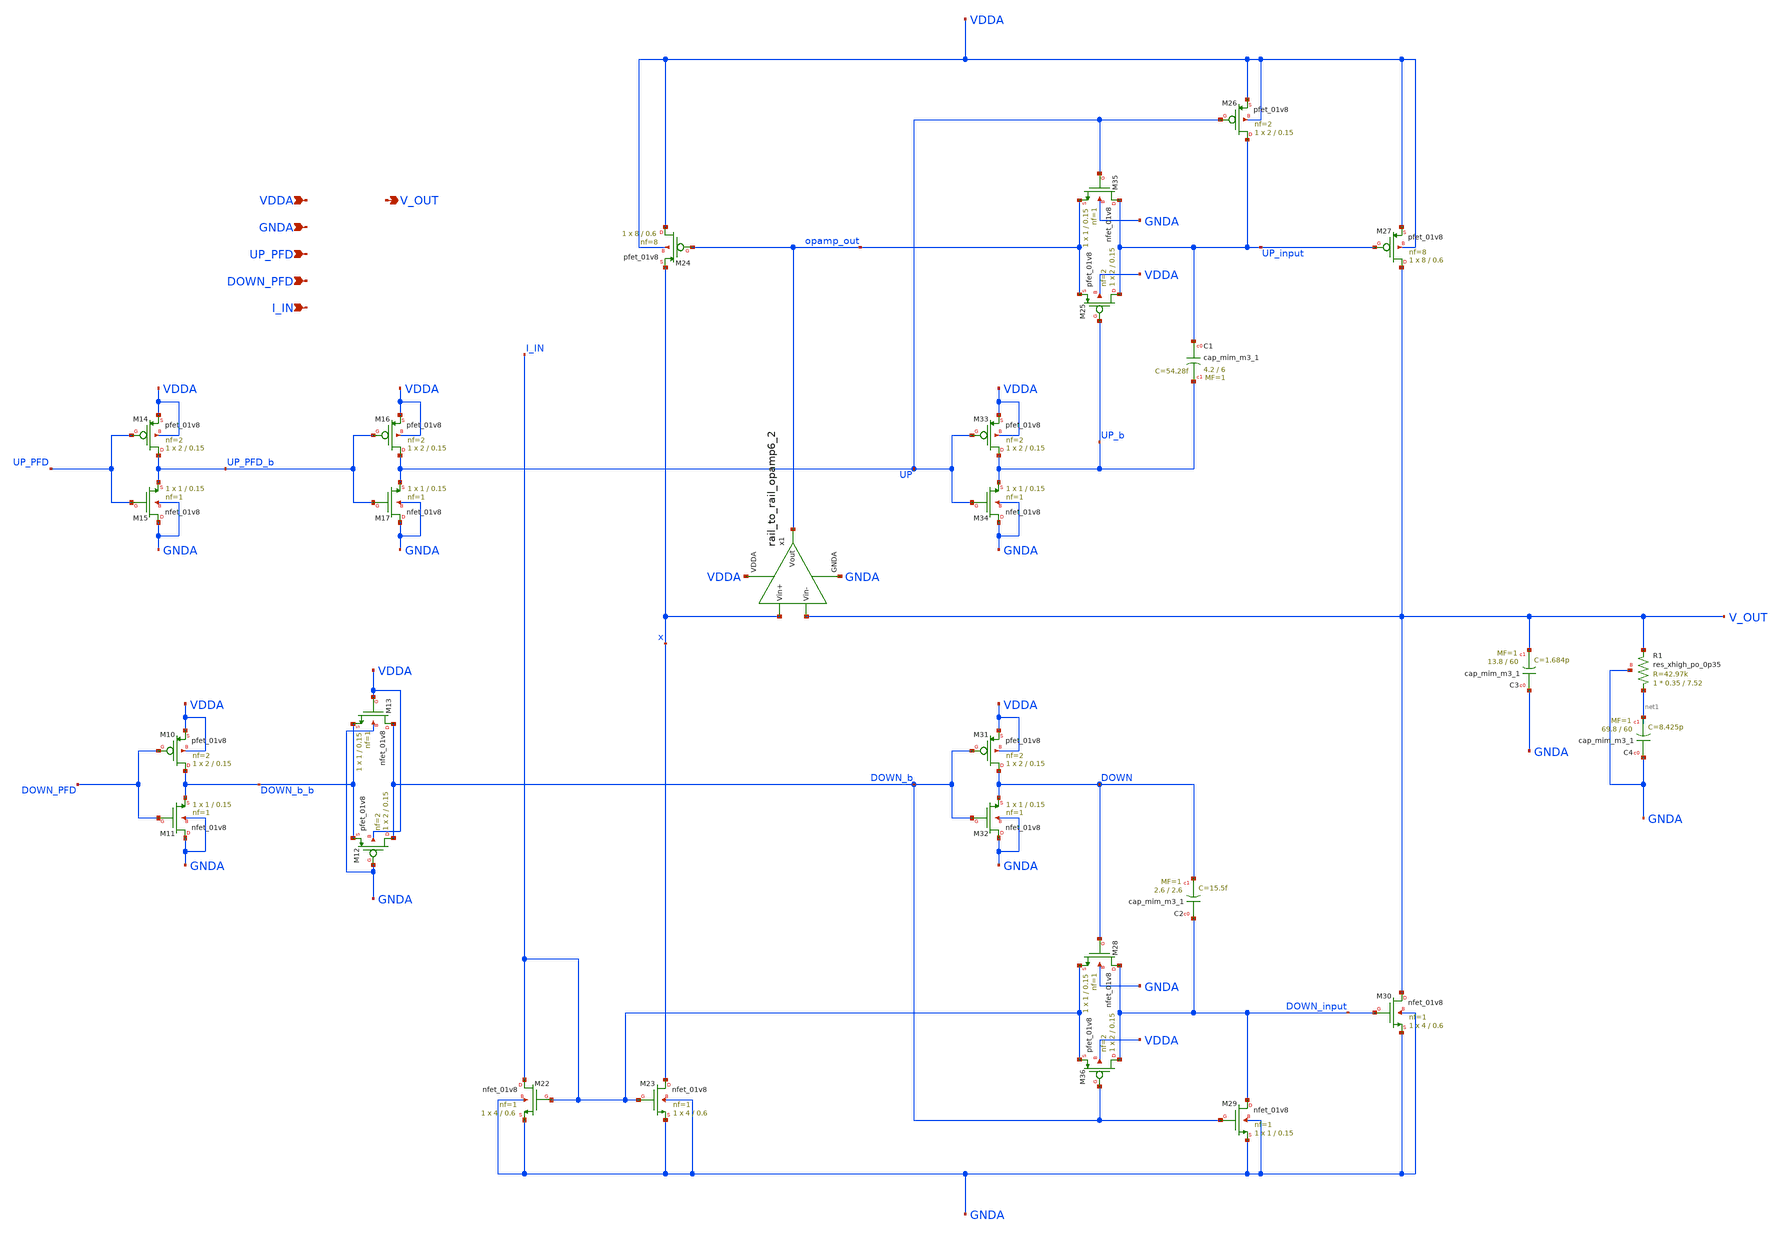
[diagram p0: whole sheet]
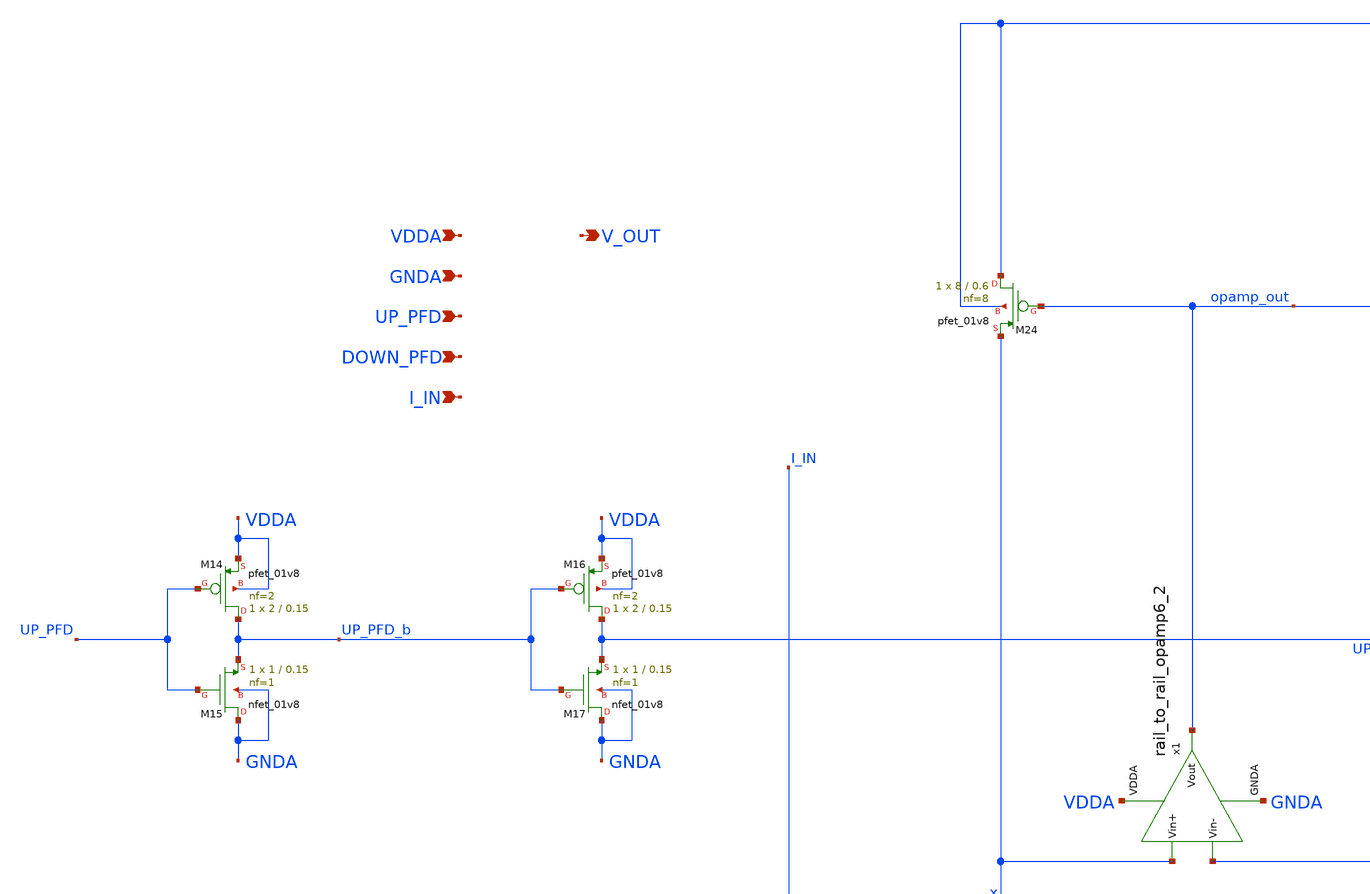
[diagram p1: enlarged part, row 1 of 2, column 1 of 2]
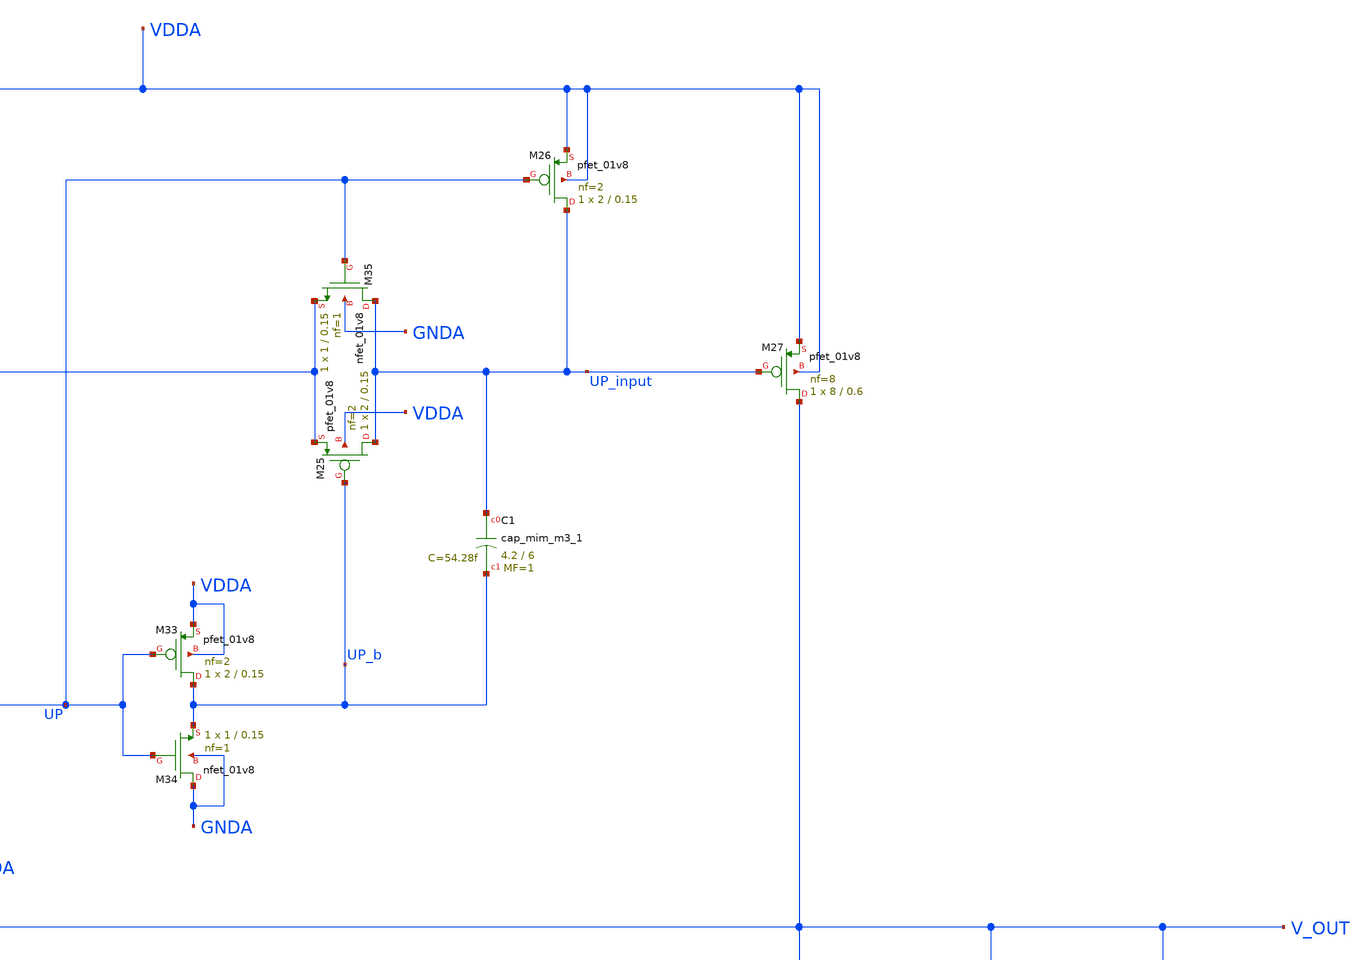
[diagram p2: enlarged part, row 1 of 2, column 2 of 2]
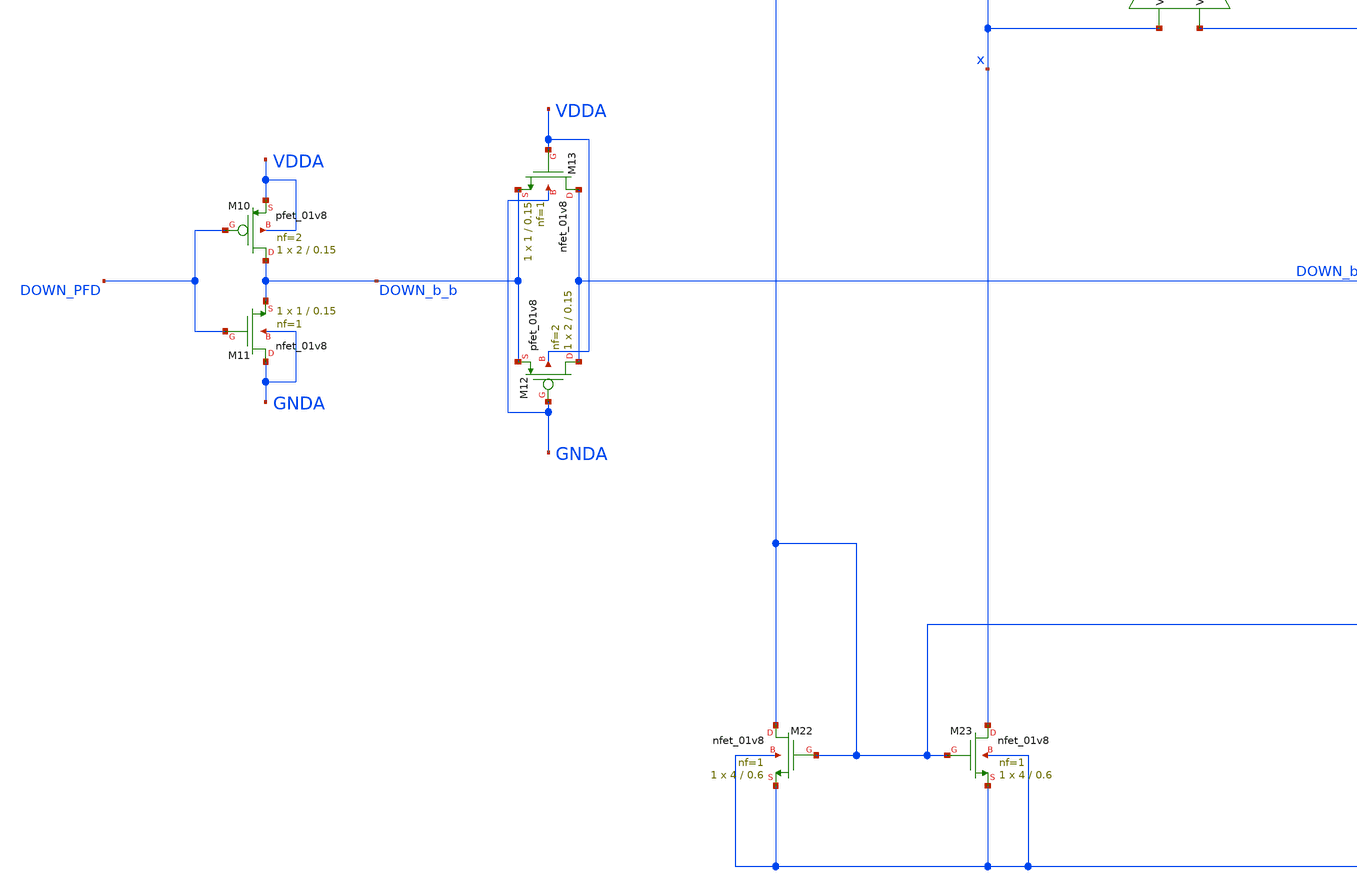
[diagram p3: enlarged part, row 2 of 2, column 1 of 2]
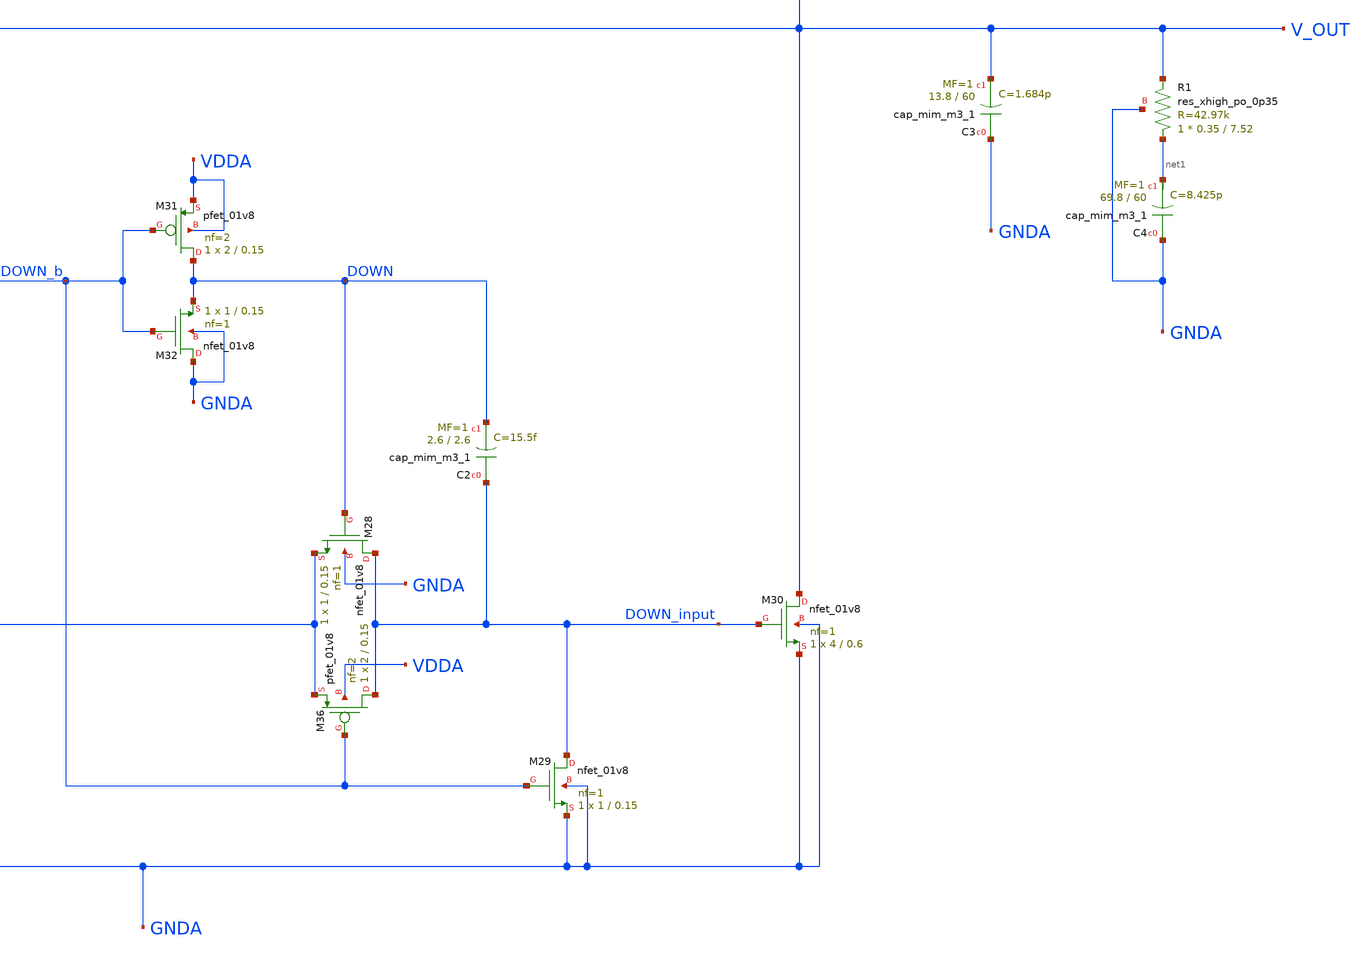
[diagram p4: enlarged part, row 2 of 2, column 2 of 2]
** sch_path: projects/pll/charge_pump/xschem_ngspice/cp_lf_xschem.sch
**.subckt cp_lf_xschem VDDA V_OUT GNDA UP_PFD DOWN_PFD I_IN
*.ipin VDDA
*.opin V_OUT
*.ipin GNDA
*.ipin UP_PFD
*.ipin DOWN_PFD
*.ipin I_IN
XM12 DOWN_b GNDA DOWN_b_b VDDA sky130_fd_pr__pfet_01v8 L=0.15 W=2 nf=2 ad='int((nf+1)/2) * W/nf * 0.29'
+ as='int((nf+2)/2) * W/nf * 0.29' pd='2*int((nf+1)/2) * (W/nf + 0.29)' ps='2*int((nf+2)/2) * (W/nf + 0.29)'
+ nrd='0.29 / W' nrs='0.29 / W' sa=0 sb=0 sd=0 mult=1 m=1
XM13 DOWN_b VDDA DOWN_b_b GNDA sky130_fd_pr__nfet_01v8 L=0.15 W=1 nf=1 ad='int((nf+1)/2) * W/nf * 0.29'
+ as='int((nf+2)/2) * W/nf * 0.29' pd='2*int((nf+1)/2) * (W/nf + 0.29)' ps='2*int((nf+2)/2) * (W/nf + 0.29)'
+ nrd='0.29 / W' nrs='0.29 / W' sa=0 sb=0 sd=0 mult=1 m=1
XM10 DOWN_b_b DOWN_PFD VDDA VDDA sky130_fd_pr__pfet_01v8 L=0.15 W=2 nf=2 ad='int((nf+1)/2) * W/nf * 0.29'
+ as='int((nf+2)/2) * W/nf * 0.29' pd='2*int((nf+1)/2) * (W/nf + 0.29)' ps='2*int((nf+2)/2) * (W/nf + 0.29)'
+ nrd='0.29 / W' nrs='0.29 / W' sa=0 sb=0 sd=0 mult=1 m=1
XM11 GNDA DOWN_PFD DOWN_b_b GNDA sky130_fd_pr__nfet_01v8 L=0.15 W=1 nf=1 ad='int((nf+1)/2) * W/nf * 0.29'
+ as='int((nf+2)/2) * W/nf * 0.29' pd='2*int((nf+1)/2) * (W/nf + 0.29)' ps='2*int((nf+2)/2) * (W/nf + 0.29)'
+ nrd='0.29 / W' nrs='0.29 / W' sa=0 sb=0 sd=0 mult=1 m=1
XM14 UP_PFD_b UP_PFD VDDA VDDA sky130_fd_pr__pfet_01v8 L=0.15 W=2 nf=2 ad='int((nf+1)/2) * W/nf * 0.29'
+ as='int((nf+2)/2) * W/nf * 0.29' pd='2*int((nf+1)/2) * (W/nf + 0.29)' ps='2*int((nf+2)/2) * (W/nf + 0.29)'
+ nrd='0.29 / W' nrs='0.29 / W' sa=0 sb=0 sd=0 mult=1 m=1
XM15 GNDA UP_PFD UP_PFD_b GNDA sky130_fd_pr__nfet_01v8 L=0.15 W=1 nf=1 ad='int((nf+1)/2) * W/nf * 0.29'
+ as='int((nf+2)/2) * W/nf * 0.29' pd='2*int((nf+1)/2) * (W/nf + 0.29)' ps='2*int((nf+2)/2) * (W/nf + 0.29)'
+ nrd='0.29 / W' nrs='0.29 / W' sa=0 sb=0 sd=0 mult=1 m=1
XM16 UP UP_PFD_b VDDA VDDA sky130_fd_pr__pfet_01v8 L=0.15 W=2 nf=2 ad='int((nf+1)/2) * W/nf * 0.29' as='int((nf+2)/2) * W/nf * 0.29'
+ pd='2*int((nf+1)/2) * (W/nf + 0.29)' ps='2*int((nf+2)/2) * (W/nf + 0.29)' nrd='0.29 / W' nrs='0.29 / W'
+ sa=0 sb=0 sd=0 mult=1 m=1
XM17 GNDA UP_PFD_b UP GNDA sky130_fd_pr__nfet_01v8 L=0.15 W=1 nf=1 ad='int((nf+1)/2) * W/nf * 0.29' as='int((nf+2)/2) * W/nf * 0.29'
+ pd='2*int((nf+1)/2) * (W/nf + 0.29)' ps='2*int((nf+2)/2) * (W/nf + 0.29)' nrd='0.29 / W' nrs='0.29 / W'
+ sa=0 sb=0 sd=0 mult=1 m=1
XM22 I_IN I_IN GNDA GNDA sky130_fd_pr__nfet_01v8 L=0.6 W=4 nf=1 ad='int((nf+1)/2) * W/nf * 0.29' as='int((nf+2)/2) * W/nf * 0.29'
+ pd='2*int((nf+1)/2) * (W/nf + 0.29)' ps='2*int((nf+2)/2) * (W/nf + 0.29)' nrd='0.29 / W' nrs='0.29 / W'
+ sa=0 sb=0 sd=0 mult=1 m=1
XM23 x I_IN GNDA GNDA sky130_fd_pr__nfet_01v8 L=0.6 W=4 nf=1 ad='int((nf+1)/2) * W/nf * 0.29' as='int((nf+2)/2) * W/nf * 0.29'
+ pd='2*int((nf+1)/2) * (W/nf + 0.29)' ps='2*int((nf+2)/2) * (W/nf + 0.29)' nrd='0.29 / W' nrs='0.29 / W'
+ sa=0 sb=0 sd=0 mult=1 m=1
XM24 VDDA opamp_out x VDDA sky130_fd_pr__pfet_01v8 L=0.6 W=8 nf=8 ad='int((nf+1)/2) * W/nf * 0.29' as='int((nf+2)/2) * W/nf * 0.29'
+ pd='2*int((nf+1)/2) * (W/nf + 0.29)' ps='2*int((nf+2)/2) * (W/nf + 0.29)' nrd='0.29 / W' nrs='0.29 / W'
+ sa=0 sb=0 sd=0 mult=1 m=1
XM25 UP_input UP_b opamp_out VDDA sky130_fd_pr__pfet_01v8 L=0.15 W=2 nf=2 ad='int((nf+1)/2) * W/nf * 0.29'
+ as='int((nf+2)/2) * W/nf * 0.29' pd='2*int((nf+1)/2) * (W/nf + 0.29)' ps='2*int((nf+2)/2) * (W/nf + 0.29)'
+ nrd='0.29 / W' nrs='0.29 / W' sa=0 sb=0 sd=0 mult=1 m=1
XM26 UP_input UP VDDA VDDA sky130_fd_pr__pfet_01v8 L=0.15 W=2 nf=2 ad='int((nf+1)/2) * W/nf * 0.29' as='int((nf+2)/2) * W/nf * 0.29'
+ pd='2*int((nf+1)/2) * (W/nf + 0.29)' ps='2*int((nf+2)/2) * (W/nf + 0.29)' nrd='0.29 / W' nrs='0.29 / W'
+ sa=0 sb=0 sd=0 mult=1 m=1
XM27 V_OUT UP_input VDDA VDDA sky130_fd_pr__pfet_01v8 L=0.6 W=8 nf=8 ad='int((nf+1)/2) * W/nf * 0.29'
+ as='int((nf+2)/2) * W/nf * 0.29' pd='2*int((nf+1)/2) * (W/nf + 0.29)' ps='2*int((nf+2)/2) * (W/nf + 0.29)'
+ nrd='0.29 / W' nrs='0.29 / W' sa=0 sb=0 sd=0 mult=1 m=1
XM28 DOWN_input DOWN I_IN GNDA sky130_fd_pr__nfet_01v8 L=0.15 W=1 nf=1 ad='int((nf+1)/2) * W/nf * 0.29'
+ as='int((nf+2)/2) * W/nf * 0.29' pd='2*int((nf+1)/2) * (W/nf + 0.29)' ps='2*int((nf+2)/2) * (W/nf + 0.29)'
+ nrd='0.29 / W' nrs='0.29 / W' sa=0 sb=0 sd=0 mult=1 m=1
XM29 DOWN_input DOWN_b GNDA GNDA sky130_fd_pr__nfet_01v8 L=0.15 W=1 nf=1 ad='int((nf+1)/2) * W/nf * 0.29'
+ as='int((nf+2)/2) * W/nf * 0.29' pd='2*int((nf+1)/2) * (W/nf + 0.29)' ps='2*int((nf+2)/2) * (W/nf + 0.29)'
+ nrd='0.29 / W' nrs='0.29 / W' sa=0 sb=0 sd=0 mult=1 m=1
XM30 V_OUT DOWN_input GNDA GNDA sky130_fd_pr__nfet_01v8 L=0.6 W=4 nf=1 ad='int((nf+1)/2) * W/nf * 0.29'
+ as='int((nf+2)/2) * W/nf * 0.29' pd='2*int((nf+1)/2) * (W/nf + 0.29)' ps='2*int((nf+2)/2) * (W/nf + 0.29)'
+ nrd='0.29 / W' nrs='0.29 / W' sa=0 sb=0 sd=0 mult=1 m=1
XM31 DOWN DOWN_b VDDA VDDA sky130_fd_pr__pfet_01v8 L=0.15 W=2 nf=2 ad='int((nf+1)/2) * W/nf * 0.29' as='int((nf+2)/2) * W/nf * 0.29'
+ pd='2*int((nf+1)/2) * (W/nf + 0.29)' ps='2*int((nf+2)/2) * (W/nf + 0.29)' nrd='0.29 / W' nrs='0.29 / W'
+ sa=0 sb=0 sd=0 mult=1 m=1
XM32 GNDA DOWN_b DOWN GNDA sky130_fd_pr__nfet_01v8 L=0.15 W=1 nf=1 ad='int((nf+1)/2) * W/nf * 0.29' as='int((nf+2)/2) * W/nf * 0.29'
+ pd='2*int((nf+1)/2) * (W/nf + 0.29)' ps='2*int((nf+2)/2) * (W/nf + 0.29)' nrd='0.29 / W' nrs='0.29 / W'
+ sa=0 sb=0 sd=0 mult=1 m=1
XM33 UP_b UP VDDA VDDA sky130_fd_pr__pfet_01v8 L=0.15 W=2 nf=2 ad='int((nf+1)/2) * W/nf * 0.29' as='int((nf+2)/2) * W/nf * 0.29'
+ pd='2*int((nf+1)/2) * (W/nf + 0.29)' ps='2*int((nf+2)/2) * (W/nf + 0.29)' nrd='0.29 / W' nrs='0.29 / W'
+ sa=0 sb=0 sd=0 mult=1 m=1
XM34 GNDA UP UP_b GNDA sky130_fd_pr__nfet_01v8 L=0.15 W=1 nf=1 ad='int((nf+1)/2) * W/nf * 0.29' as='int((nf+2)/2) * W/nf * 0.29'
+ pd='2*int((nf+1)/2) * (W/nf + 0.29)' ps='2*int((nf+2)/2) * (W/nf + 0.29)' nrd='0.29 / W' nrs='0.29 / W'
+ sa=0 sb=0 sd=0 mult=1 m=1
XM35 UP_input UP opamp_out GNDA sky130_fd_pr__nfet_01v8 L=0.15 W=1 nf=1 ad='int((nf+1)/2) * W/nf * 0.29'
+ as='int((nf+2)/2) * W/nf * 0.29' pd='2*int((nf+1)/2) * (W/nf + 0.29)' ps='2*int((nf+2)/2) * (W/nf + 0.29)'
+ nrd='0.29 / W' nrs='0.29 / W' sa=0 sb=0 sd=0 mult=1 m=1
XM36 DOWN_input DOWN_b I_IN VDDA sky130_fd_pr__pfet_01v8 L=0.15 W=2 nf=2 ad='int((nf+1)/2) * W/nf * 0.29'
+ as='int((nf+2)/2) * W/nf * 0.29' pd='2*int((nf+1)/2) * (W/nf + 0.29)' ps='2*int((nf+2)/2) * (W/nf + 0.29)'
+ nrd='0.29 / W' nrs='0.29 / W' sa=0 sb=0 sd=0 mult=1 m=1
XC1 UP_input UP_b sky130_fd_pr__cap_mim_m3_1 W=4.2 L=6 MF=1 m=1
XC2 DOWN_input DOWN sky130_fd_pr__cap_mim_m3_1 W=2.6 L=2.6 MF=1 m=1
XC3 GNDA V_OUT sky130_fd_pr__cap_mim_m3_1 W=13.8 L=60 MF=1 m=1
XC4 GNDA net1 sky130_fd_pr__cap_mim_m3_1 W=69.8 L=60 MF=1 m=1
XR1 net1 V_OUT GNDA sky130_fd_pr__res_xhigh_po_0p35 L=7.52 mult=1 m=1
x1 VDDA x V_OUT opamp_out GNDA rail_to_rail_opamp6_2
**.ends

* expanding   symbol:
*+  /foss/designs/my_design/projects/pll/charge_pump/xschem_ngspice/rail_to_rail_opamp6_2.sym # of pins=5
** sym_path: projects/pll/charge_pump/xschem_ngspice/rail_to_rail_opamp6_2.sym
** sch_path: projects/pll/charge_pump/xschem_ngspice/rail_to_rail_opamp6_2.sch
.subckt rail_to_rail_opamp6_2 VDDA Vin+ Vin- Vout GNDA
*.opin Vout
*.ipin Vin+
*.ipin Vin-
*.ipin VDDA
*.ipin GNDA
XM2 n_left Vin- v_common_n GNDA sky130_fd_pr__nfet_01v8 L=0.15 W=1 nf=1 ad='int((nf+1)/2) * W/nf * 0.29'
+ as='int((nf+2)/2) * W/nf * 0.29' pd='2*int((nf+1)/2) * (W/nf + 0.29)' ps='2*int((nf+2)/2) * (W/nf + 0.29)'
+ nrd='0.29 / W' nrs='0.29 / W' sa=0 sb=0 sd=0 mult=1 m=1
XM3 n_right Vin+ v_common_n GNDA sky130_fd_pr__nfet_01v8 L=0.15 W=1 nf=1 ad='int((nf+1)/2) * W/nf * 0.29'
+ as='int((nf+2)/2) * W/nf * 0.29' pd='2*int((nf+1)/2) * (W/nf + 0.29)' ps='2*int((nf+2)/2) * (W/nf + 0.29)'
+ nrd='0.29 / W' nrs='0.29 / W' sa=0 sb=0 sd=0 mult=1 m=1
XM5 n_left n_left VDDA VDDA sky130_fd_pr__pfet_01v8 L=0.15 W=2 nf=2 ad='int((nf+1)/2) * W/nf * 0.29'
+ as='int((nf+2)/2) * W/nf * 0.29' pd='2*int((nf+1)/2) * (W/nf + 0.29)' ps='2*int((nf+2)/2) * (W/nf + 0.29)'
+ nrd='0.29 / W' nrs='0.29 / W' sa=0 sb=0 sd=0 mult=1 m=1
XM4 n_right n_left VDDA VDDA sky130_fd_pr__pfet_01v8 L=0.15 W=2 nf=2 ad='int((nf+1)/2) * W/nf * 0.29'
+ as='int((nf+2)/2) * W/nf * 0.29' pd='2*int((nf+1)/2) * (W/nf + 0.29)' ps='2*int((nf+2)/2) * (W/nf + 0.29)'
+ nrd='0.29 / W' nrs='0.29 / W' sa=0 sb=0 sd=0 mult=1 m=1
XM6 v_common_p p_bias VDDA VDDA sky130_fd_pr__pfet_01v8 L=0.5 W=10 nf=2 ad='int((nf+1)/2) * W/nf * 0.29'
+ as='int((nf+2)/2) * W/nf * 0.29' pd='2*int((nf+1)/2) * (W/nf + 0.29)' ps='2*int((nf+2)/2) * (W/nf + 0.29)'
+ nrd='0.29 / W' nrs='0.29 / W' sa=0 sb=0 sd=0 mult=1 m=1
XM7 p_left Vin- v_common_p VDDA sky130_fd_pr__pfet_01v8 L=0.15 W=2 nf=2 ad='int((nf+1)/2) * W/nf * 0.29'
+ as='int((nf+2)/2) * W/nf * 0.29' pd='2*int((nf+1)/2) * (W/nf + 0.29)' ps='2*int((nf+2)/2) * (W/nf + 0.29)'
+ nrd='0.29 / W' nrs='0.29 / W' sa=0 sb=0 sd=0 mult=1 m=1
XM8 p_right Vin+ v_common_p VDDA sky130_fd_pr__pfet_01v8 L=0.15 W=2 nf=2 ad='int((nf+1)/2) * W/nf * 0.29'
+ as='int((nf+2)/2) * W/nf * 0.29' pd='2*int((nf+1)/2) * (W/nf + 0.29)' ps='2*int((nf+2)/2) * (W/nf + 0.29)'
+ nrd='0.29 / W' nrs='0.29 / W' sa=0 sb=0 sd=0 mult=1 m=1
XM9 p_left p_left GNDA GNDA sky130_fd_pr__nfet_01v8 L=0.15 W=1 nf=1 ad='int((nf+1)/2) * W/nf * 0.29'
+ as='int((nf+2)/2) * W/nf * 0.29' pd='2*int((nf+1)/2) * (W/nf + 0.29)' ps='2*int((nf+2)/2) * (W/nf + 0.29)'
+ nrd='0.29 / W' nrs='0.29 / W' sa=0 sb=0 sd=0 mult=1 m=1
XM10 p_right p_left GNDA GNDA sky130_fd_pr__nfet_01v8 L=0.15 W=1 nf=1 ad='int((nf+1)/2) * W/nf * 0.29'
+ as='int((nf+2)/2) * W/nf * 0.29' pd='2*int((nf+1)/2) * (W/nf + 0.29)' ps='2*int((nf+2)/2) * (W/nf + 0.29)'
+ nrd='0.29 / W' nrs='0.29 / W' sa=0 sb=0 sd=0 mult=1 m=1
XM1 v_common_n n_bias GNDA GNDA sky130_fd_pr__nfet_01v8 L=0.5 W=5 nf=1 ad='int((nf+1)/2) * W/nf * 0.29'
+ as='int((nf+2)/2) * W/nf * 0.29' pd='2*int((nf+1)/2) * (W/nf + 0.29)' ps='2*int((nf+2)/2) * (W/nf + 0.29)'
+ nrd='0.29 / W' nrs='0.29 / W' sa=0 sb=0 sd=0 mult=1 m=1
XM11 Vout n_right VDDA VDDA sky130_fd_pr__pfet_01v8 L=0.15 W=4 nf=2 ad='int((nf+1)/2) * W/nf * 0.29'
+ as='int((nf+2)/2) * W/nf * 0.29' pd='2*int((nf+1)/2) * (W/nf + 0.29)' ps='2*int((nf+2)/2) * (W/nf + 0.29)'
+ nrd='0.29 / W' nrs='0.29 / W' sa=0 sb=0 sd=0 mult=1 m=1
XM12 Vout p_right GNDA GNDA sky130_fd_pr__nfet_01v8 L=0.15 W=2 nf=1 ad='int((nf+1)/2) * W/nf * 0.29'
+ as='int((nf+2)/2) * W/nf * 0.29' pd='2*int((nf+1)/2) * (W/nf + 0.29)' ps='2*int((nf+2)/2) * (W/nf + 0.29)'
+ nrd='0.29 / W' nrs='0.29 / W' sa=0 sb=0 sd=0 mult=1 m=1
XM13 n_bias n_bias GNDA GNDA sky130_fd_pr__nfet_01v8 L=0.5 W=5 nf=1 ad='int((nf+1)/2) * W/nf * 0.29'
+ as='int((nf+2)/2) * W/nf * 0.29' pd='2*int((nf+1)/2) * (W/nf + 0.29)' ps='2*int((nf+2)/2) * (W/nf + 0.29)'
+ nrd='0.29 / W' nrs='0.29 / W' sa=0 sb=0 sd=0 mult=1 m=1
XM14 p_bias p_bias VDDA VDDA sky130_fd_pr__pfet_01v8 L=0.5 W=10 nf=2 ad='int((nf+1)/2) * W/nf * 0.29'
+ as='int((nf+2)/2) * W/nf * 0.29' pd='2*int((nf+1)/2) * (W/nf + 0.29)' ps='2*int((nf+2)/2) * (W/nf + 0.29)'
+ nrd='0.29 / W' nrs='0.29 / W' sa=0 sb=0 sd=0 mult=1 m=1
XC1 Vout net1 sky130_fd_pr__cap_mim_m3_1 W=10 L=10 MF=1 m=1
XC2 Vout net2 sky130_fd_pr__cap_mim_m3_1 W=10 L=10 MF=1 m=1
XR1 net1 n_right GNDA sky130_fd_pr__res_xhigh_po_0p35 L=1.14 mult=1 m=1
XR2 net2 p_right GNDA sky130_fd_pr__res_xhigh_po_0p35 L=0.86 mult=1 m=1
XR4 n_bias p_bias GNDA sky130_fd_pr__res_xhigh_po_2p85 L=0.5 mult=1 m=1
.ends

.end
